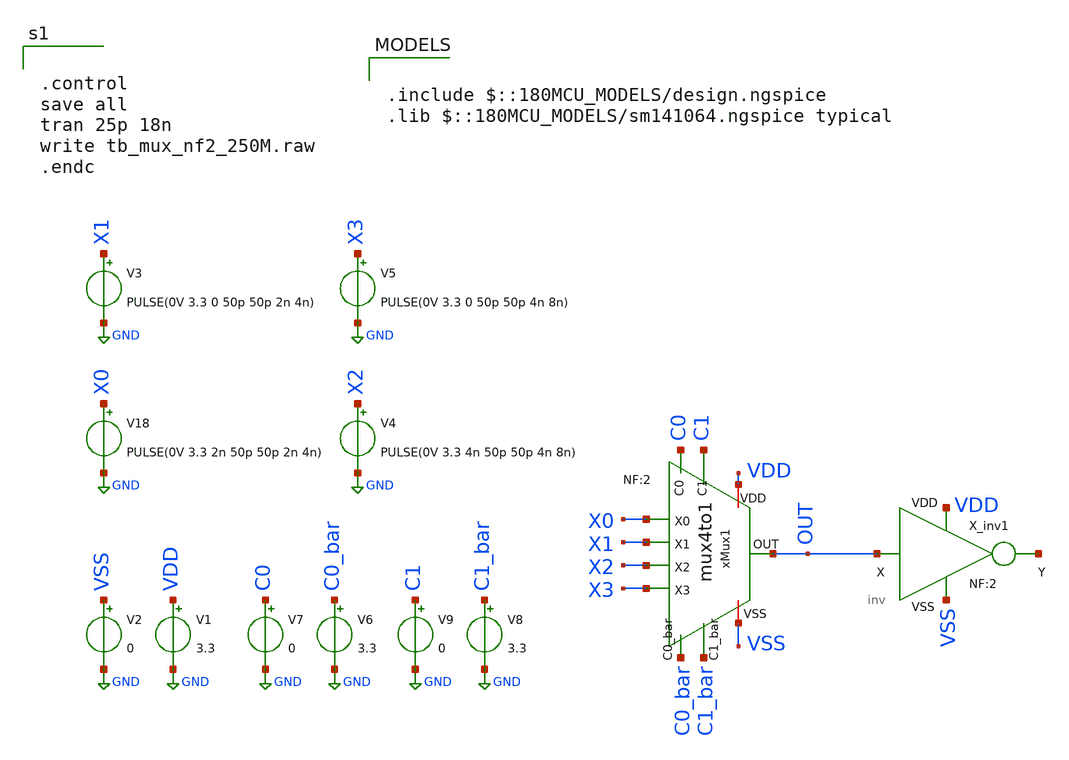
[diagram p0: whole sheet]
** sch_path: xschem_lib/DFFRAM_full_custom/tb_MUX4to1.sch
**.subckt tb_MUX4to1
xMux1 VDD VSS C0_bar C0 C1 C1_bar X0 X1 OUT X2 X3 mux4to1 NF=2
V1 VDD GND 3.3
V2 VSS GND 0
V18 X0 GND PULSE(0V 3.3 2n 50p 50p 2n 4n)
V3 X1 GND PULSE(0V 3.3 0 50p 50p 2n 4n)
V4 X2 GND PULSE(0V 3.3 4n 50p 50p 4n 8n)
V5 X3 GND PULSE(0V 3.3 0 50p 50p 4n 8n)
V6 C0_bar GND 3.3
V7 C0 GND 0
V8 C1_bar GND 3.3
V9 C1 GND 0
X_inv1 OUT VDD VSS net1 inv NF=2
**** begin user architecture code


.control
save all
tran 25p 18n
write tb_mux_nf2_250M.raw
.endc



.include $::180MCU_MODELS/design.ngspice
.lib $::180MCU_MODELS/sm141064.ngspice typical

**** end user architecture code
**.ends

* expanding   symbol:  xschem_lib/DFFRAM_full_custom/mux4to1.sym # of pins=11
** sym_path: xschem_lib/DFFRAM_full_custom/mux4to1.sym
** sch_path: xschem_lib/DFFRAM_full_custom/mux4to1.sch
.subckt mux4to1 VDD VSS C0_bar C0 C1 C1_bar X0 X1 OUT X2 X3  NF=2
*.ipin C0
*.ipin C0_bar
*.ipin C1_bar
*.ipin C1
*.ipin X0
*.ipin X1
*.ipin X2
*.ipin X3
*.opin OUT
*.iopin VDD
*.iopin VSS
xTr1 X1 VDD C0_bar VSS C0 net2 tr_gate NF=2
xTr2 X0 VDD C0 VSS C0_bar net2 tr_gate NF=2
xTr3 X3 VDD C0_bar VSS C0 net1 tr_gate NF=2
xTr4 X2 VDD C0 VSS C0_bar net1 tr_gate NF=2
xTr5 net1 VDD C1_bar VSS C1 OUT tr_gate NF=2
xTr7 net2 VDD C1 VSS C1_bar OUT tr_gate NF=2
.ends


* expanding   symbol:  xschem_lib/DFFRAM_full_custom/inv.sym # of pins=4
** sym_path: xschem_lib/DFFRAM_full_custom/inv.sym
** sch_path: xschem_lib/DFFRAM_full_custom/inv.sch
.subckt inv X VDD VSS Y  NF=2
*.iopin VSS
*.ipin X
*.opin Y
*.iopin VDD
XM1 Y X VSS VSS nfet_03v3 L=0.28u W=NF*0.85u nf=NF ad='int((nf+1)/2) * W/nf * 0.18u' as='int((nf+2)/2) * W/nf * 0.18u'
+ pd='2*int((nf+1)/2) * (W/nf + 0.18u)' ps='2*int((nf+2)/2) * (W/nf + 0.18u)' nrd='0.18u / W' nrs='0.18u / W'
+ sa=0 sb=0 sd=0 m=1
XM2 Y X VDD VDD pfet_03v3 L=0.28u W=NF*1.7u nf=NF ad='int((nf+1)/2) * W/nf * 0.18u' as='int((nf+2)/2) * W/nf * 0.18u'
+ pd='2*int((nf+1)/2) * (W/nf + 0.18u)' ps='2*int((nf+2)/2) * (W/nf + 0.18u)' nrd='0.18u / W' nrs='0.18u / W'
+ sa=0 sb=0 sd=0 m=1
.ends


* expanding   symbol:  xschem_lib/DFFRAM_full_custom/tr_gate.sym # of pins=6
** sym_path: xschem_lib/DFFRAM_full_custom/tr_gate.sym
** sch_path: xschem_lib/DFFRAM_full_custom/tr_gate.sch
.subckt tr_gate X VDD A_bar VSS A Y  NF=2
*.iopin VSS
*.ipin A_bar
*.iopin VDD
*.ipin A
*.iopin X
*.iopin Y
XM1 X A Y VSS nfet_03v3 L=0.28u W=NF*0.85u nf=NF ad='int((nf+1)/2) * W/nf * 0.18u' as='int((nf+2)/2) * W/nf * 0.18u'
+ pd='2*int((nf+1)/2) * (W/nf + 0.18u)' ps='2*int((nf+2)/2) * (W/nf + 0.18u)' nrd='0.18u / W' nrs='0.18u / W'
+ sa=0 sb=0 sd=0 m=1
XM2 Y A_bar X VDD pfet_03v3 L=0.28u W=NF*1.7u nf=NF ad='int((nf+1)/2) * W/nf * 0.18u' as='int((nf+2)/2) * W/nf * 0.18u'
+ pd='2*int((nf+1)/2) * (W/nf + 0.18u)' ps='2*int((nf+2)/2) * (W/nf + 0.18u)' nrd='0.18u / W' nrs='0.18u / W'
+ sa=0 sb=0 sd=0 m=1
.ends

.GLOBAL GND
.end
